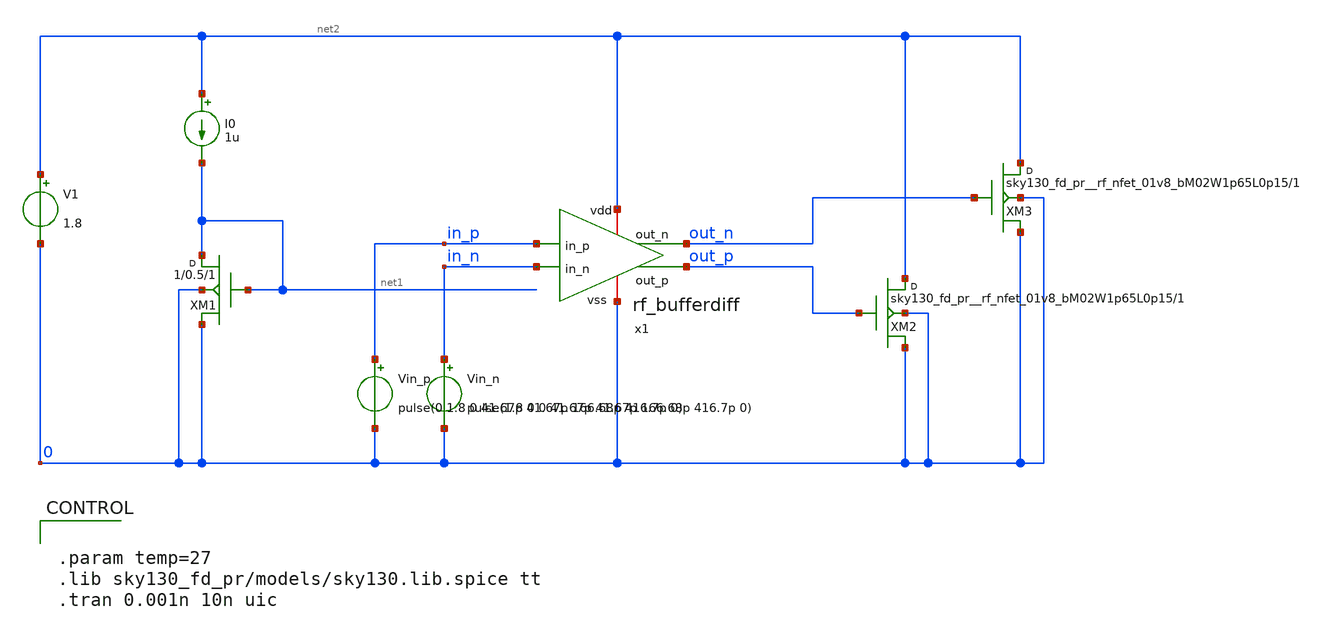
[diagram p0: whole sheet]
** sch_path: design/rf_bufferdiff/test/rf_bufferdiff_tb.sch
**.subckt rf_bufferdiff_tb
x1 net2 out_n out_p in_p in_n 0 rf_bufferdiff
XM1 net1 net1 0 0 sky130_fd_pr__nfet_01v8 w=1 l=0.5 m=1
Vin_n in_n 0 pulse(1.8 0 0 41.67p 41.67p 166.68p 416.7p 0)
Vin_p in_p 0 pulse(0 1.8 0 41.67p 41.67p 166.68p 416.7p 0)
I0 net2 net1 1u
V1 net2 0 1.8
XXM2 net2 out_p 0 0 sky130_fd_pr__rf_nfet_01v8_bM02W1p65L0p15 m=1
XXM3 net2 out_n 0 0 sky130_fd_pr__rf_nfet_01v8_bM02W1p65L0p15 m=1
**** begin user architecture code


.param temp=27
.lib sky130_fd_pr/models/sky130.lib.spice tt
.tran 0.001n 10n uic


**** end user architecture code
**.ends

* expanding   symbol:  rf_bufferdiff/rf_bufferdiff.sym # of pins=6
** sym_path: design/rf_bufferdiff/rf_bufferdiff.sym
** sch_path: design/rf_bufferdiff/rf_bufferdiff.sch
.subckt rf_bufferdiff vdd out_n out_p in_p in_n vss
*.iopin vdd
*.iopin vss
*.ipin in_p
*.ipin in_n
*.opin out_n
*.opin out_p
XXMdiffp out_n in_p vss vss sky130_fd_pr__rf_nfet_01v8_bM02W1p65L0p15 m=1
XXMdiffn out_p in_n vss vss sky130_fd_pr__rf_nfet_01v8_bM02W1p65L0p15 m=1
XRn vdd out_n vss sky130_fd_pr__res_xhigh_po_2p85 m=1
XRp vdd out_p vss sky130_fd_pr__res_xhigh_po_2p85 m=1
.ends

.end
